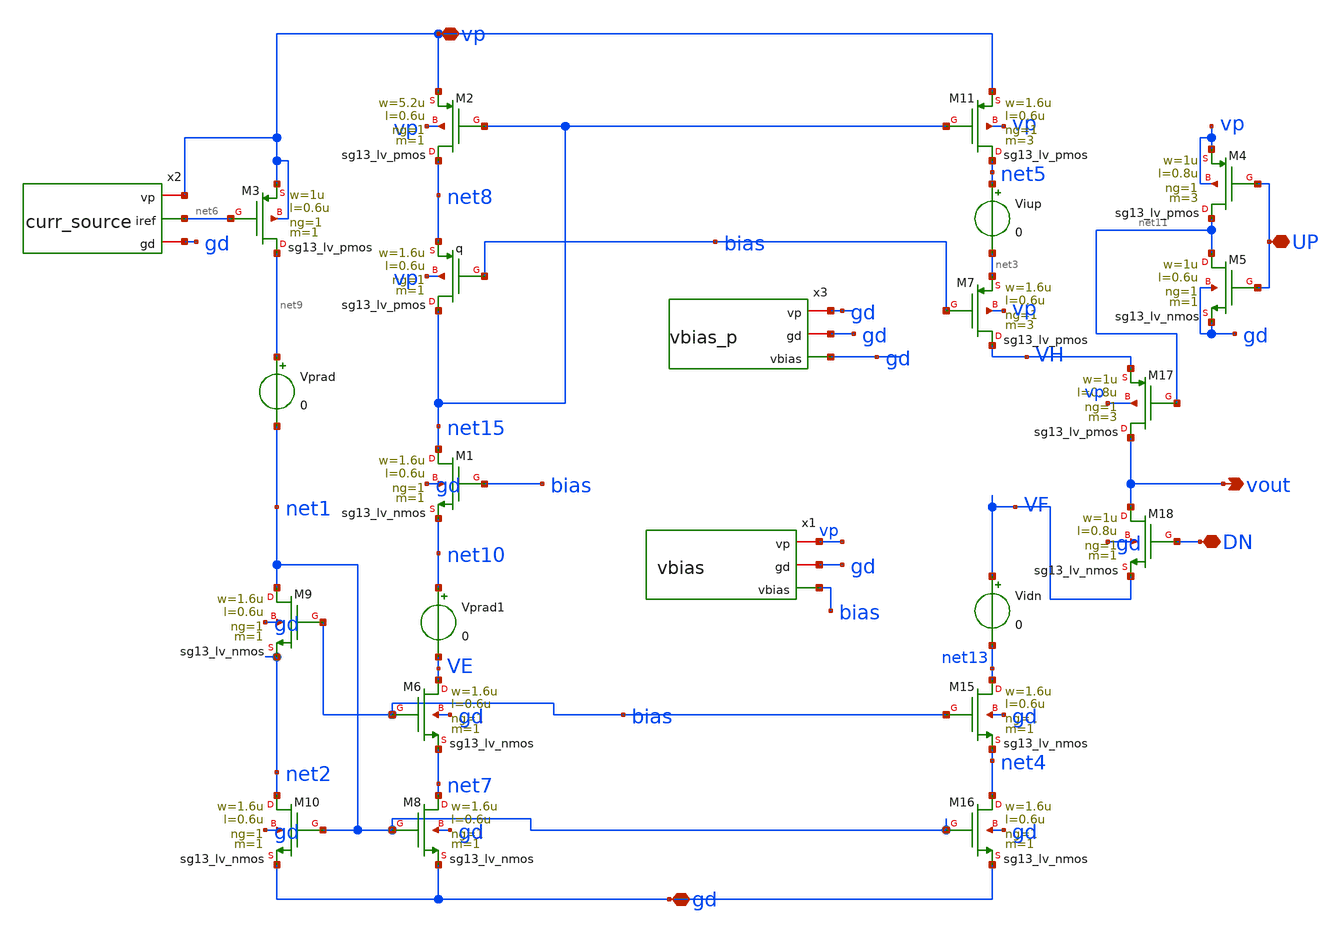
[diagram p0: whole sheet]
** sch_path: schematics/charge_pump/NEW_500n_cp_cell.sch
**.subckt NEW_500n_cp_cell DN gd vp vout UP
*.iopin DN
*.iopin gd
*.iopin vp
*.opin vout
*.iopin UP
XM15 net13 bias net4 gd sg13_lv_nmos w=1.6u l=0.6u ng=1 m=1 mm_ok=1
XM16 net4 net1 gd gd sg13_lv_nmos w=1.6u l=0.6u ng=1 m=1 mm_ok=1
XM1 net15 bias net10 gd sg13_lv_nmos w=1.6u l=0.6u ng=1 m=1 mm_ok=1
XM6 VE bias net7 gd sg13_lv_nmos w=1.6u l=0.6u ng=1 m=1 mm_ok=1
XM8 net7 net1 gd gd sg13_lv_nmos w=1.6u l=0.6u ng=1 m=1 mm_ok=1
XM9 net1 bias net2 gd sg13_lv_nmos w=1.6u l=0.6u ng=1 m=1 mm_ok=1
XM10 net2 net1 gd gd sg13_lv_nmos w=1.6u l=0.6u ng=1 m=1 mm_ok=1
Vprad net9 net1 0
Vprad1 net10 VE 0
Vidn VF net13 0
Xq net15 bias net8 vp sg13_lv_pmos w=1.6u l=0.6u ng=1 m=1 mm_ok=1
XM7 VH bias net3 vp sg13_lv_pmos w=1.6u l=0.6u ng=1 m=3 mm_ok=1
XM11 net5 net15 vp vp sg13_lv_pmos w=1.6u l=0.6u ng=1 m=3 mm_ok=1
XM2 net8 net15 vp vp sg13_lv_pmos w=5.2u l=0.6u ng=1 m=1 mm_ok=1
XM17 vout net11 VH vp sg13_lv_pmos w=1u l=0.8u ng=1 m=3 mm_ok=1
XM18 vout DN VF gd sg13_lv_nmos w=1u l=0.8u ng=1 m=1 mm_ok=1
x1 vp gd bias vbias
Viup net5 net3 0
XM3 net9 net6 vp vp sg13_lv_pmos w=1u l=0.6u ng=1 m=1 mm_ok=1
x2 vp net6 gd curr_source
x3 gd gd gd vbias_p
XM4 net11 UP vp vp sg13_lv_pmos w=1u l=0.8u ng=1 m=3 mm_ok=1
XM5 net11 UP gd gd sg13_lv_nmos w=1u l=0.6u ng=1 m=1 mm_ok=1
**.ends
.end
